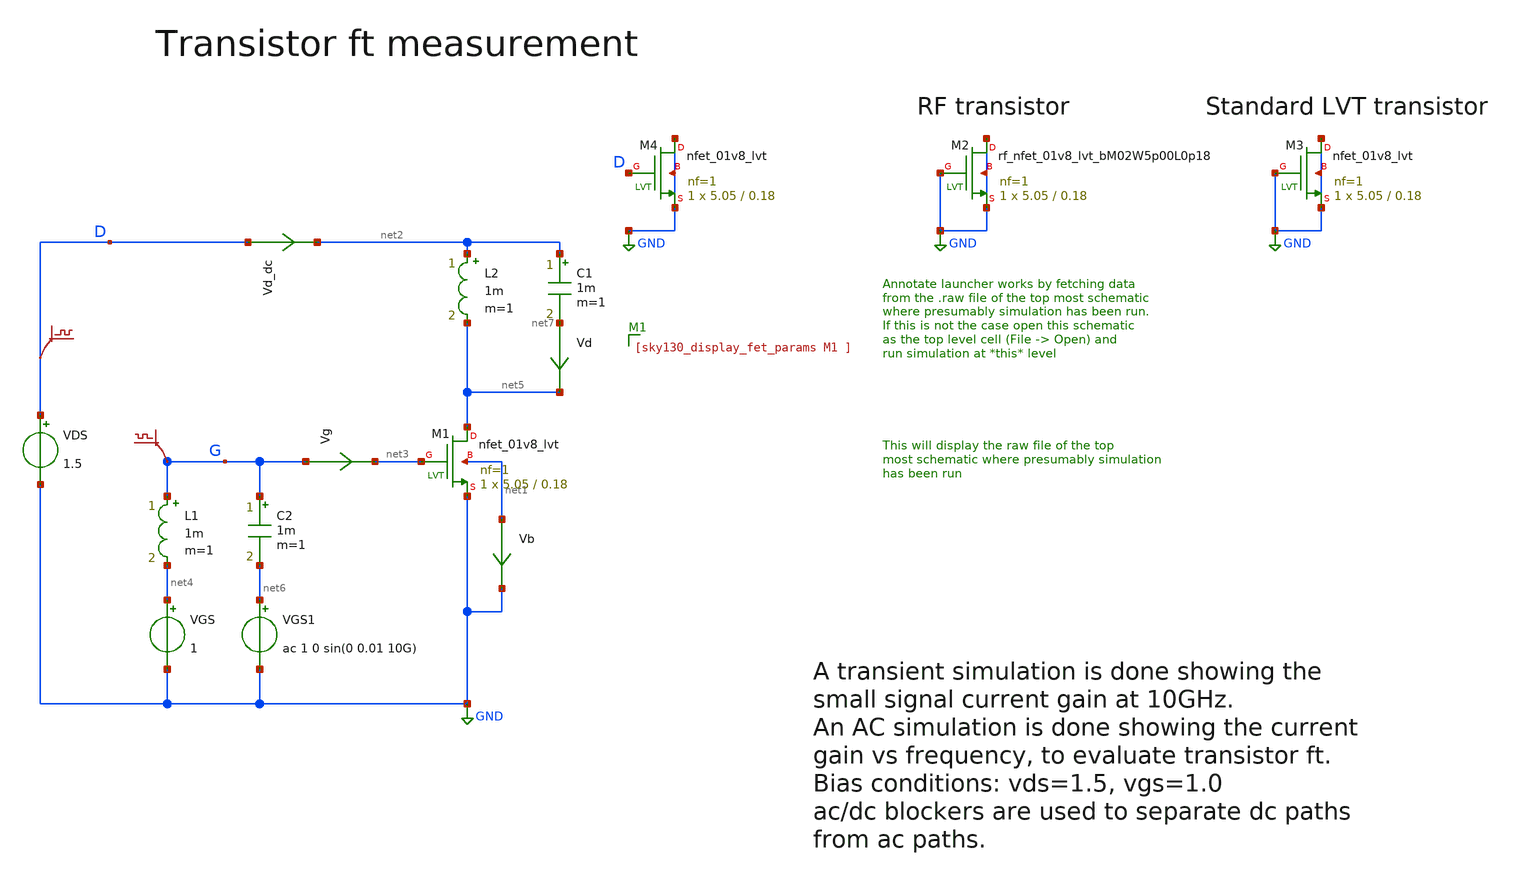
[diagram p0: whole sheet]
** sch_path: sky130A/xschem_libs/sky130_tests_ase/tb_ft_test_2/schematic/tb_ft_test_2.sch
* Copyright 2021 Stefan Frederik Schippers
* Licensed under the Apache License, Version 2.0 (the "License");
* you may not use this file except in compliance with the License.
* You may obtain a copy of the License at
* https://www.apache.org/licenses/LICENSE-2.0
* Unless required by applicable law or agreed to in writing, software
* distributed under the License is distributed on an "AS IS" BASIS,
* WITHOUT WARRANTIES OR CONDITIONS OF ANY KIND, either express or implied.
* See the License for the specific language governing permissions and
* limitations under the License.
**.subckt tb_ft_test_2
VDS D GND 1.5
VGS net4 GND 1
Vd net7 net5 0
.save i(vd)
L1 G net4 1m m=1
Vg G net3 0
.save i(vg)
L2 net2 net5 1m m=1
C1 net2 net7 1m m=1
C2 G net6 1m m=1
VGS1 net6 GND ac 1 0 sin(0 0.01 10G)
Vd_dc D net2 0
.save i(vd_dc)
.save v(g)
.save v(d)
Vb net1 GND 0
.save i(vb)
XM2 GND GND GND GND sky130_fd_pr__rf_nfet_01v8_lvt_bM02W5p00L0p18 L=0.18 W=5.05 nf=1 ad='int((1 + 1)/2) * 5.05 / 1 * 0.29'
+ as='int((1 + 2)/2) * 5.05 / 1 * 0.29' pd='2*int((1 + 1)/2) * (5.05 / 1 + 0.29)' ps='2*int((1 + 2)/2) * (5.05 / 1 + 0.29)'
+ nrd='0.29 / 5.05 ' nrs='0.29 / 5.05 ' sa=0 sb=0 sd=0 mult=1 m=1
XM3 GND GND GND GND sky130_fd_pr__nfet_01v8_lvt L=0.18 W=5.05 nf=1 ad='int((1 + 1)/2) * 5.05 / 1 * 0.29'
+ as='int((1 + 2)/2) * 5.05 / 1 * 0.29' pd='2*int((1 + 1)/2) * (5.05 / 1 + 0.29)' ps='2*int((1 + 2)/2) * (5.05 / 1 + 0.29)'
+ nrd='0.29 / 5.05 ' nrs='0.29 / 5.05 ' sa=0 sb=0 sd=0 mult=1 m=1
XM1 net5 net3 GND net1 sky130_fd_pr__nfet_01v8_lvt L=0.18 W=5.05 nf=1 ad='int((1 + 1)/2) * 5.05 / 1 * 0.29'
+ as='int((1 + 2)/2) * 5.05 / 1 * 0.29' pd='2*int((1 + 1)/2) * (5.05 / 1 + 0.29)' ps='2*int((1 + 2)/2) * (5.05 / 1 + 0.29)'
+ nrd='0.29 / 5.05 ' nrs='0.29 / 5.05 ' sa=0 sb=0 sd=0 mult=1 m=1
XM4 GND D GND GND sky130_fd_pr__nfet_01v8_lvt L=0.18 W=5.05 nf=1 ad='int((1 + 1)/2) * 5.05 / 1 * 0.29'
+ as='int((1 + 2)/2) * 5.05 / 1 * 0.29' pd='2*int((1 + 1)/2) * (5.05 / 1 + 0.29)' ps='2*int((1 + 2)/2) * (5.05 / 1 + 0.29)'
+ nrd='0.29 / 5.05 ' nrs='0.29 / 5.05 ' sa=0 sb=0 sd=0 mult=1 m=1
**.ends
.GLOBAL GND
.end
